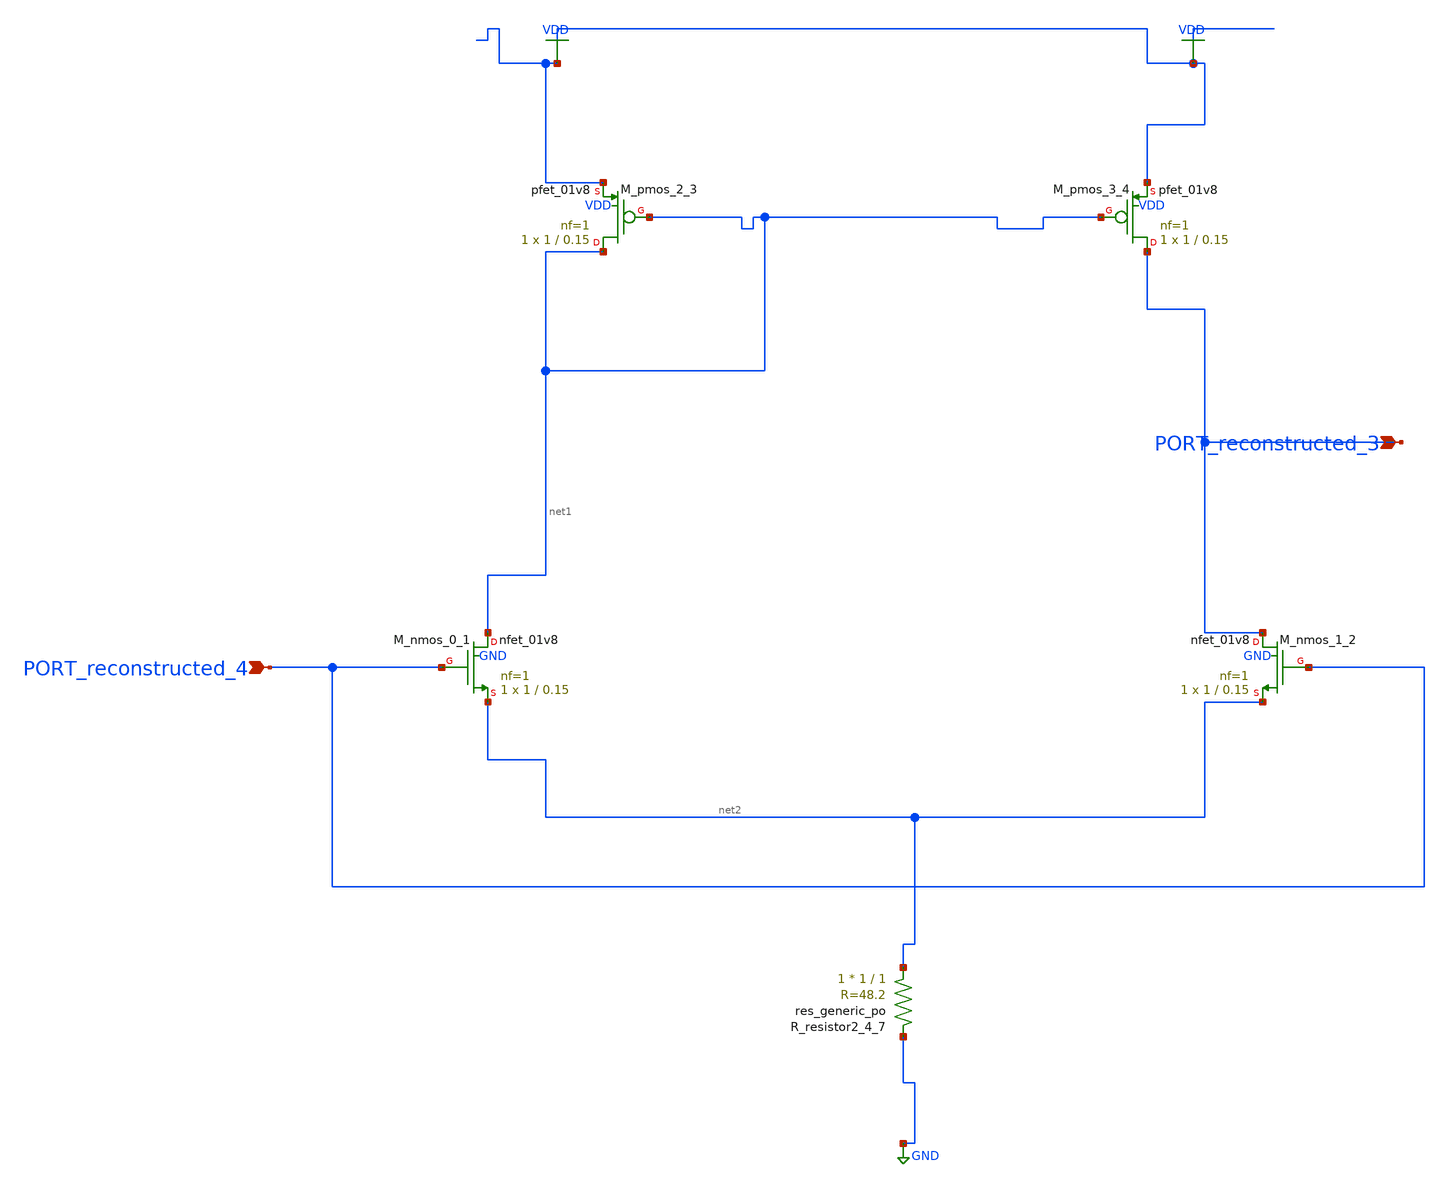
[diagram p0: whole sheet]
** sch_path: schematics/AMSNet/290.sch
**.subckt 290 PORT_reconstructed_3 PORT_reconstructed_4
*.ipin PORT_reconstructed_3
*.ipin PORT_reconstructed_4
XM_nmos_0_1 net1 PORT_reconstructed_4 net2 GND sky130_fd_pr__nfet_01v8 L=0.15 W=1 nf=1 ad='int((1 + 1)/2) * 1 / 1 * 0.29'
+ as='int((1 + 2)/2) * 1 / 1 * 0.29' pd='2*int((1 + 1)/2) * (1 / 1 + 0.29)' ps='2*int((1 + 2)/2) * (1 / 1 + 0.29)'
+ nrd='0.29 / 1 ' nrs='0.29 / 1 ' sa=0 sb=0 sd=0 mult=1 m=1
XM_nmos_1_2 PORT_reconstructed_3 PORT_reconstructed_4 net2 GND sky130_fd_pr__nfet_01v8 L=0.15 W=1 nf=1
+ ad='int((1 + 1)/2) * 1 / 1 * 0.29' as='int((1 + 2)/2) * 1 / 1 * 0.29' pd='2*int((1 + 1)/2) * (1 / 1 + 0.29)'
+ ps='2*int((1 + 2)/2) * (1 / 1 + 0.29)' nrd='0.29 / 1 ' nrs='0.29 / 1 ' sa=0 sb=0 sd=0 mult=1 m=1
XM_pmos_2_3 net1 net1 VDD VDD sky130_fd_pr__pfet_01v8 L=0.15 W=1 nf=1 ad='int((1 + 1)/2) * 1 / 1 * 0.29'
+ as='int((1 + 2)/2) * 1 / 1 * 0.29' pd='2*int((1 + 1)/2) * (1 / 1 + 0.29)' ps='2*int((1 + 2)/2) * (1 / 1 + 0.29)'
+ nrd='0.29 / 1 ' nrs='0.29 / 1 ' sa=0 sb=0 sd=0 mult=1 m=1
XM_pmos_3_4 PORT_reconstructed_3 net1 VDD VDD sky130_fd_pr__pfet_01v8 L=0.15 W=1 nf=1 ad='int((1 + 1)/2) * 1 / 1 * 0.29'
+ as='int((1 + 2)/2) * 1 / 1 * 0.29' pd='2*int((1 + 1)/2) * (1 / 1 + 0.29)' ps='2*int((1 + 2)/2) * (1 / 1 + 0.29)'
+ nrd='0.29 / 1 ' nrs='0.29 / 1 ' sa=0 sb=0 sd=0 mult=1 m=1
XR_resistor2_4_7 net2 GND sky130_fd_pr__res_generic_po W=1 L=1 m=1
**.ends
.GLOBAL GND
.GLOBAL VDD
.end
